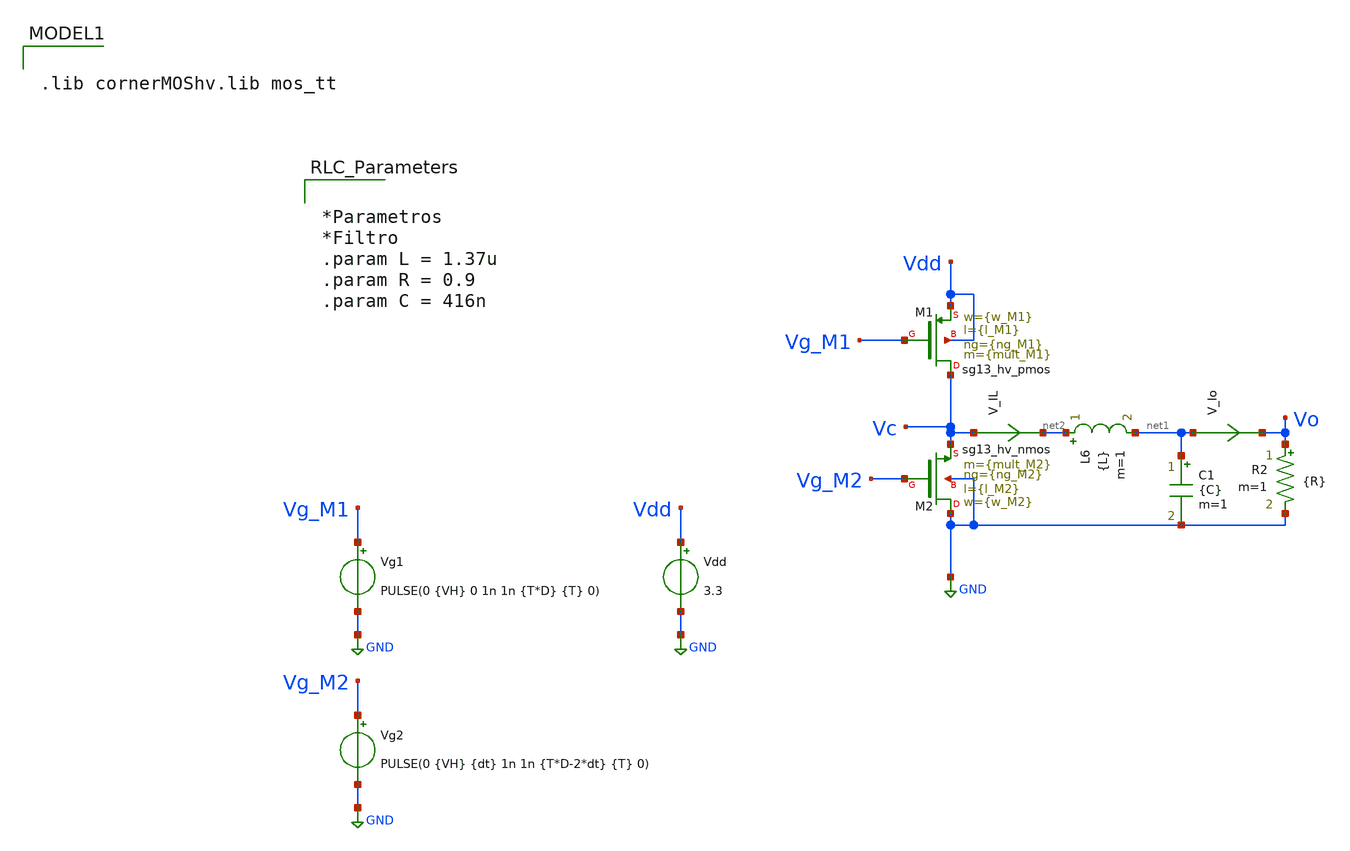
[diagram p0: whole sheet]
** sch_path: xschem/TB_DCDCBuck_V2.sch
**.subckt TB_DCDCBuck_V2
Vdd Vdd GND 3.3
Vg2 Vg_M2 GND PULSE(0 {VH} {dt} 1n 1n {T*D-2*dt} {T} 0)
Vg1 Vg_M1 GND PULSE(0 {VH} 0 1n 1n {T*D} {T} 0)
XM2 GND Vg_M2 Vc GND sg13_hv_nmos w={w_M2} l={l_M2} ng={ng_M2} m={mult_M2} mm_ok=1
XM1 Vc Vg_M1 Vdd Vdd sg13_hv_pmos w={w_M1} l={l_M1} ng={ng_M1} m={mult_M1} mm_ok=1
L6 net2 net1 {L} m=1
C1 net1 GND {C} m=1
V_Io net1 Vo 0
.save i(v_io)
V_IL Vc net2 0
.save i(v_il)
R2 Vo GND {R} m=1
**** begin user architecture code


*Parametros
*Filtro
.param L = 1.37u
.param R = 0.9
.param C = 416n





.param temp=27
*.param mult_M1 = 2400
.param mult_M1 = 3600
.param w_M1 =10u
*.param l_M1 = 0.2u ** Posee mayor capacidad de corriente, pero en sub-umbral conduce mucha
*+ corriente
.param l_M1 = 0.22u
.param ng_M1 = 1

*.param mult_M2 = 1200
.param mult_M2 = 1800
.param w_M2 =10u
*.param l_M2 =0.25u
.param l_M2 =0.25u
.param ng_M2 =1








.param VH = 3
.param D = 0.42
.param T = 1u
.param dt = 5n
.param temp = 27






.save all
.control
reset
set color0 = white
tran 1n 100u
plot i(V_Io) i(V_IL)
plot v(Vo)
plot v(Vc)
plot v(Vg_M1) v(Vg_M2)
.endc

.end



.lib cornerMOShv.lib mos_tt

**** end user architecture code
**.ends
.GLOBAL GND
.end
